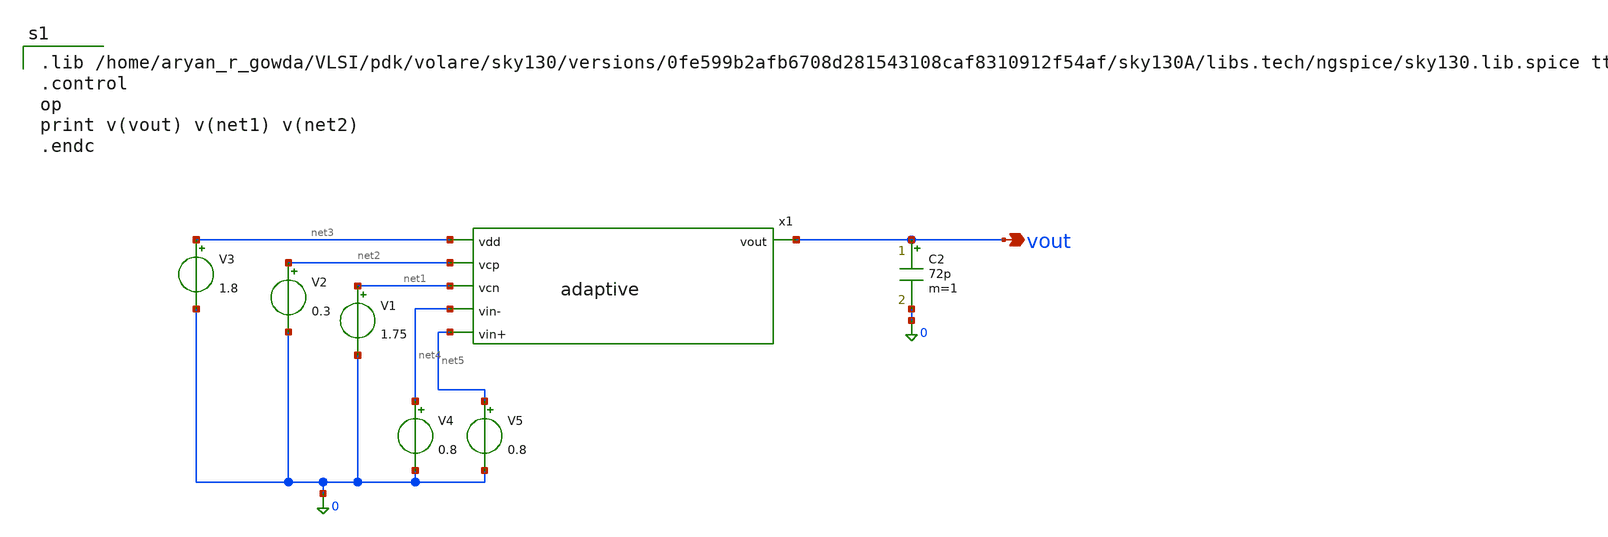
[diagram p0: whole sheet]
** sch_path: schematic/adaptive_test.sch
**.subckt adaptive_test vout
*.opin vout
V1 net1 0 1.75
V2 net2 0 0.3
V3 net3 0 1.8
C2 vout 0 72p m=1
V4 net4 0 0.8
V5 net5 0 0.8
x1 net3 net2 net1 vout net4 net5 adaptive
**** begin user architecture code

.lib /home/aryan_r_gowda/VLSI/pdk/volare/sky130/versions/0fe599b2afb6708d281543108caf8310912f54af/sky130A/libs.tech/ngspice/sky130.lib.spice tt
.control
op
print v(vout) v(net1) v(net2)
.endc


**** end user architecture code
**.ends

* expanding   symbol:  adaptive.sym # of pins=6
** sym_path: schematic/adaptive.sym
** sch_path: schematic/adaptive.sch
.subckt adaptive vdd vcp vcn vout vin- vin+
*.ipin vin+
*.ipin vin-
*.ipin vdd
*.ipin vcp
*.ipin vcn
*.opin vout
XM1B y vin+ net2 VDD sky130_fd_pr__pfet_01v8 L=0.15 W=1 nf=1 ad='int((nf+1)/2) * W/nf * 0.29' as='int((nf+2)/2) * W/nf * 0.29'
+ pd='2*int((nf+1)/2) * (W/nf + 0.29)' ps='2*int((nf+2)/2) * (W/nf + 0.29)' nrd='0.29 / W' nrs='0.29 / W'
+ sa=0 sb=0 sd=0 mult=1 m=1
XM2A x vin- net1 VDD sky130_fd_pr__pfet_01v8 L=0.15 W=1 nf=1 ad='int((nf+1)/2) * W/nf * 0.29' as='int((nf+2)/2) * W/nf * 0.29'
+ pd='2*int((nf+1)/2) * (W/nf + 0.29)' ps='2*int((nf+2)/2) * (W/nf + 0.29)' nrd='0.29 / W' nrs='0.29 / W'
+ sa=0 sb=0 sd=0 mult=1 m=1
XM1A net11 vin+ net2 VDD sky130_fd_pr__pfet_01v8 L=0.15 W=1 nf=1 ad='int((nf+1)/2) * W/nf * 0.29' as='int((nf+2)/2) * W/nf * 0.29'
+ pd='2*int((nf+1)/2) * (W/nf + 0.29)' ps='2*int((nf+2)/2) * (W/nf + 0.29)' nrd='0.29 / W' nrs='0.29 / W'
+ sa=0 sb=0 sd=0 mult=1 m=1
XM2B net12 vin- net1 VDD sky130_fd_pr__pfet_01v8 L=0.15 W=1 nf=1 ad='int((nf+1)/2) * W/nf * 0.29' as='int((nf+2)/2) * W/nf * 0.29'
+ pd='2*int((nf+1)/2) * (W/nf + 0.29)' ps='2*int((nf+2)/2) * (W/nf + 0.29)' nrd='0.29 / W' nrs='0.29 / W'
+ sa=0 sb=0 sd=0 mult=1 m=1
XM16 0 net6 net4 VDD sky130_fd_pr__pfet_01v8 L=0.15 W=1 nf=1 ad='int((nf+1)/2) * W/nf * 0.29' as='int((nf+2)/2) * W/nf * 0.29'
+ pd='2*int((nf+1)/2) * (W/nf + 0.29)' ps='2*int((nf+2)/2) * (W/nf + 0.29)' nrd='0.29 / W' nrs='0.29 / W'
+ sa=0 sb=0 sd=0 mult=1 m=1
XM12 net6 vin- net2 VDD sky130_fd_pr__pfet_01v8 L=0.15 W=1 nf=1 ad='int((nf+1)/2) * W/nf * 0.29' as='int((nf+2)/2) * W/nf * 0.29'
+ pd='2*int((nf+1)/2) * (W/nf + 0.29)' ps='2*int((nf+2)/2) * (W/nf + 0.29)' nrd='0.29 / W' nrs='0.29 / W'
+ sa=0 sb=0 sd=0 mult=1 m=1
XM1 net5 vin+ net1 VDD sky130_fd_pr__pfet_01v8 L=0.15 W=1 nf=1 ad='int((nf+1)/2) * W/nf * 0.29' as='int((nf+2)/2) * W/nf * 0.29'
+ pd='2*int((nf+1)/2) * (W/nf + 0.29)' ps='2*int((nf+2)/2) * (W/nf + 0.29)' nrd='0.29 / W' nrs='0.29 / W'
+ sa=0 sb=0 sd=0 mult=1 m=1
XM13 net1 net3 vdd VDD sky130_fd_pr__pfet_01v8 L=0.15 W=1 nf=1 ad='int((nf+1)/2) * W/nf * 0.29' as='int((nf+2)/2) * W/nf * 0.29'
+ pd='2*int((nf+1)/2) * (W/nf + 0.29)' ps='2*int((nf+2)/2) * (W/nf + 0.29)' nrd='0.29 / W' nrs='0.29 / W'
+ sa=0 sb=0 sd=0 mult=1 m=1
XM14 net2 net4 vdd VDD sky130_fd_pr__pfet_01v8 L=0.15 W=1 nf=1 ad='int((nf+1)/2) * W/nf * 0.29' as='int((nf+2)/2) * W/nf * 0.29'
+ pd='2*int((nf+1)/2) * (W/nf + 0.29)' ps='2*int((nf+2)/2) * (W/nf + 0.29)' nrd='0.29 / W' nrs='0.29 / W'
+ sa=0 sb=0 sd=0 mult=1 m=1
XM15 0 net5 net3 VDD sky130_fd_pr__pfet_01v8 L=0.15 W=1 nf=1 ad='int((nf+1)/2) * W/nf * 0.29' as='int((nf+2)/2) * W/nf * 0.29'
+ pd='2*int((nf+1)/2) * (W/nf + 0.29)' ps='2*int((nf+2)/2) * (W/nf + 0.29)' nrd='0.29 / W' nrs='0.29 / W'
+ sa=0 sb=0 sd=0 mult=1 m=1
I0 vdd net3 0.2u
I1 net5 0 1u
I2 net6 0 1u
I3 vdd net4 0.2u
XM2 net11 x 0 GND sky130_fd_pr__nfet_01v8 L=0.15 W=1 nf=1 ad='int((nf+1)/2) * W/nf * 0.29' as='int((nf+2)/2) * W/nf * 0.29'
+ pd='2*int((nf+1)/2) * (W/nf + 0.29)' ps='2*int((nf+2)/2) * (W/nf + 0.29)' nrd='0.29 / W' nrs='0.29 / W'
+ sa=0 sb=0 sd=0 mult=1 m=1
XM3 net7 y 0 GND sky130_fd_pr__nfet_01v8 L=0.15 W=1 nf=1 ad='int((nf+1)/2) * W/nf * 0.29' as='int((nf+2)/2) * W/nf * 0.29'
+ pd='2*int((nf+1)/2) * (W/nf + 0.29)' ps='2*int((nf+2)/2) * (W/nf + 0.29)' nrd='0.29 / W' nrs='0.29 / W'
+ sa=0 sb=0 sd=0 mult=1 m=1
XM4 net8 z 0 GND sky130_fd_pr__nfet_01v8 L=0.15 W=1 nf=1 ad='int((nf+1)/2) * W/nf * 0.29' as='int((nf+2)/2) * W/nf * 0.29'
+ pd='2*int((nf+1)/2) * (W/nf + 0.29)' ps='2*int((nf+2)/2) * (W/nf + 0.29)' nrd='0.29 / W' nrs='0.29 / W'
+ sa=0 sb=0 sd=0 mult=1 m=1
XM5 net9 z 0 GND sky130_fd_pr__nfet_01v8 L=0.15 W=1 nf=1 ad='int((nf+1)/2) * W/nf * 0.29' as='int((nf+2)/2) * W/nf * 0.29'
+ pd='2*int((nf+1)/2) * (W/nf + 0.29)' ps='2*int((nf+2)/2) * (W/nf + 0.29)' nrd='0.29 / W' nrs='0.29 / W'
+ sa=0 sb=0 sd=0 mult=1 m=1
XM6 net10 x 0 GND sky130_fd_pr__nfet_01v8 L=0.15 W=1 nf=1 ad='int((nf+1)/2) * W/nf * 0.29' as='int((nf+2)/2) * W/nf * 0.29'
+ pd='2*int((nf+1)/2) * (W/nf + 0.29)' ps='2*int((nf+2)/2) * (W/nf + 0.29)' nrd='0.29 / W' nrs='0.29 / W'
+ sa=0 sb=0 sd=0 mult=1 m=1
XM7 net12 y 0 GND sky130_fd_pr__nfet_01v8 L=0.15 W=1 nf=1 ad='int((nf+1)/2) * W/nf * 0.29' as='int((nf+2)/2) * W/nf * 0.29'
+ pd='2*int((nf+1)/2) * (W/nf + 0.29)' ps='2*int((nf+2)/2) * (W/nf + 0.29)' nrd='0.29 / W' nrs='0.29 / W'
+ sa=0 sb=0 sd=0 mult=1 m=1
XM8 net13 net16 net11 GND sky130_fd_pr__nfet_01v8 L=0.15 W=1 nf=1 ad='int((nf+1)/2) * W/nf * 0.29' as='int((nf+2)/2) * W/nf * 0.29'
+ pd='2*int((nf+1)/2) * (W/nf + 0.29)' ps='2*int((nf+2)/2) * (W/nf + 0.29)' nrd='0.29 / W' nrs='0.29 / W'
+ sa=0 sb=0 sd=0 mult=1 m=1
XM9 x vcn net7 GND sky130_fd_pr__nfet_01v8 L=0.15 W=1 nf=1 ad='int((nf+1)/2) * W/nf * 0.29' as='int((nf+2)/2) * W/nf * 0.29'
+ pd='2*int((nf+1)/2) * (W/nf + 0.29)' ps='2*int((nf+2)/2) * (W/nf + 0.29)' nrd='0.29 / W' nrs='0.29 / W'
+ sa=0 sb=0 sd=0 mult=1 m=1
XM10 y vcn net9 GND sky130_fd_pr__nfet_01v8 L=0.15 W=1 nf=1 ad='int((nf+1)/2) * W/nf * 0.29' as='int((nf+2)/2) * W/nf * 0.29'
+ pd='2*int((nf+1)/2) * (W/nf + 0.29)' ps='2*int((nf+2)/2) * (W/nf + 0.29)' nrd='0.29 / W' nrs='0.29 / W'
+ sa=0 sb=0 sd=0 mult=1 m=1
XM11 x vcn net8 GND sky130_fd_pr__nfet_01v8 L=0.15 W=1 nf=1 ad='int((nf+1)/2) * W/nf * 0.29' as='int((nf+2)/2) * W/nf * 0.29'
+ pd='2*int((nf+1)/2) * (W/nf + 0.29)' ps='2*int((nf+2)/2) * (W/nf + 0.29)' nrd='0.29 / W' nrs='0.29 / W'
+ sa=0 sb=0 sd=0 mult=1 m=1
XM17 y vcn net10 GND sky130_fd_pr__nfet_01v8 L=0.15 W=1 nf=1 ad='int((nf+1)/2) * W/nf * 0.29' as='int((nf+2)/2) * W/nf * 0.29'
+ pd='2*int((nf+1)/2) * (W/nf + 0.29)' ps='2*int((nf+2)/2) * (W/nf + 0.29)' nrd='0.29 / W' nrs='0.29 / W'
+ sa=0 sb=0 sd=0 mult=1 m=1
XM18 vout net17 net12 GND sky130_fd_pr__nfet_01v8 L=0.15 W=6 nf=1 ad='int((nf+1)/2) * W/nf * 0.29' as='int((nf+2)/2) * W/nf * 0.29'
+ pd='2*int((nf+1)/2) * (W/nf + 0.29)' ps='2*int((nf+2)/2) * (W/nf + 0.29)' nrd='0.29 / W' nrs='0.29 / W'
+ sa=0 sb=0 sd=0 mult=1 m=1
XM25 vcp vcn net18 GND sky130_fd_pr__nfet_01v8 L=0.15 W=1 nf=1 ad='int((nf+1)/2) * W/nf * 0.29' as='int((nf+2)/2) * W/nf * 0.29'
+ pd='2*int((nf+1)/2) * (W/nf + 0.29)' ps='2*int((nf+2)/2) * (W/nf + 0.29)' nrd='0.29 / W' nrs='0.29 / W'
+ sa=0 sb=0 sd=0 mult=1 m=1
XM26 net13 net18 net14 VDD sky130_fd_pr__pfet_01v8 L=0.15 W=1 nf=1 ad='int((nf+1)/2) * W/nf * 0.29' as='int((nf+2)/2) * W/nf * 0.29'
+ pd='2*int((nf+1)/2) * (W/nf + 0.29)' ps='2*int((nf+2)/2) * (W/nf + 0.29)' nrd='0.29 / W' nrs='0.29 / W'
+ sa=0 sb=0 sd=0 mult=1 m=1
XM27 net14 net13 vdd VDD sky130_fd_pr__pfet_01v8 L=0.15 W=1 nf=1 ad='int((nf+1)/2) * W/nf * 0.29' as='int((nf+2)/2) * W/nf * 0.29'
+ pd='2*int((nf+1)/2) * (W/nf + 0.29)' ps='2*int((nf+2)/2) * (W/nf + 0.29)' nrd='0.29 / W' nrs='0.29 / W'
+ sa=0 sb=0 sd=0 mult=1 m=1
XM28 net15 net13 vdd VDD sky130_fd_pr__pfet_01v8 L=0.15 W=1 nf=1 ad='int((nf+1)/2) * W/nf * 0.29' as='int((nf+2)/2) * W/nf * 0.29'
+ pd='2*int((nf+1)/2) * (W/nf + 0.29)' ps='2*int((nf+2)/2) * (W/nf + 0.29)' nrd='0.29 / W' nrs='0.29 / W'
+ sa=0 sb=0 sd=0 mult=1 m=1
XM29 net16 z vcn VDD sky130_fd_pr__pfet_01v8 L=0.15 W=1 nf=1 ad='int((nf+1)/2) * W/nf * 0.29' as='int((nf+2)/2) * W/nf * 0.29'
+ pd='2*int((nf+1)/2) * (W/nf + 0.29)' ps='2*int((nf+2)/2) * (W/nf + 0.29)' nrd='0.29 / W' nrs='0.29 / W'
+ sa=0 sb=0 sd=0 mult=1 m=1
XM30 net17 x vcn VDD sky130_fd_pr__pfet_01v8 L=0.15 W=1 nf=1 ad='int((nf+1)/2) * W/nf * 0.29' as='int((nf+2)/2) * W/nf * 0.29'
+ pd='2*int((nf+1)/2) * (W/nf + 0.29)' ps='2*int((nf+2)/2) * (W/nf + 0.29)' nrd='0.29 / W' nrs='0.29 / W'
+ sa=0 sb=0 sd=0 mult=1 m=1
XM31 vout net18 net15 VDD sky130_fd_pr__pfet_01v8 L=0.15 W=1 nf=1 ad='int((nf+1)/2) * W/nf * 0.29' as='int((nf+2)/2) * W/nf * 0.29'
+ pd='2*int((nf+1)/2) * (W/nf + 0.29)' ps='2*int((nf+2)/2) * (W/nf + 0.29)' nrd='0.29 / W' nrs='0.29 / W'
+ sa=0 sb=0 sd=0 mult=1 m=1
C1 net16 x 500f m=1
C2 net17 y 500f m=1
C3 net13 net18 500f m=1
R1 z x 52k m=1
R4 y z 52k m=1
.ends

.end
